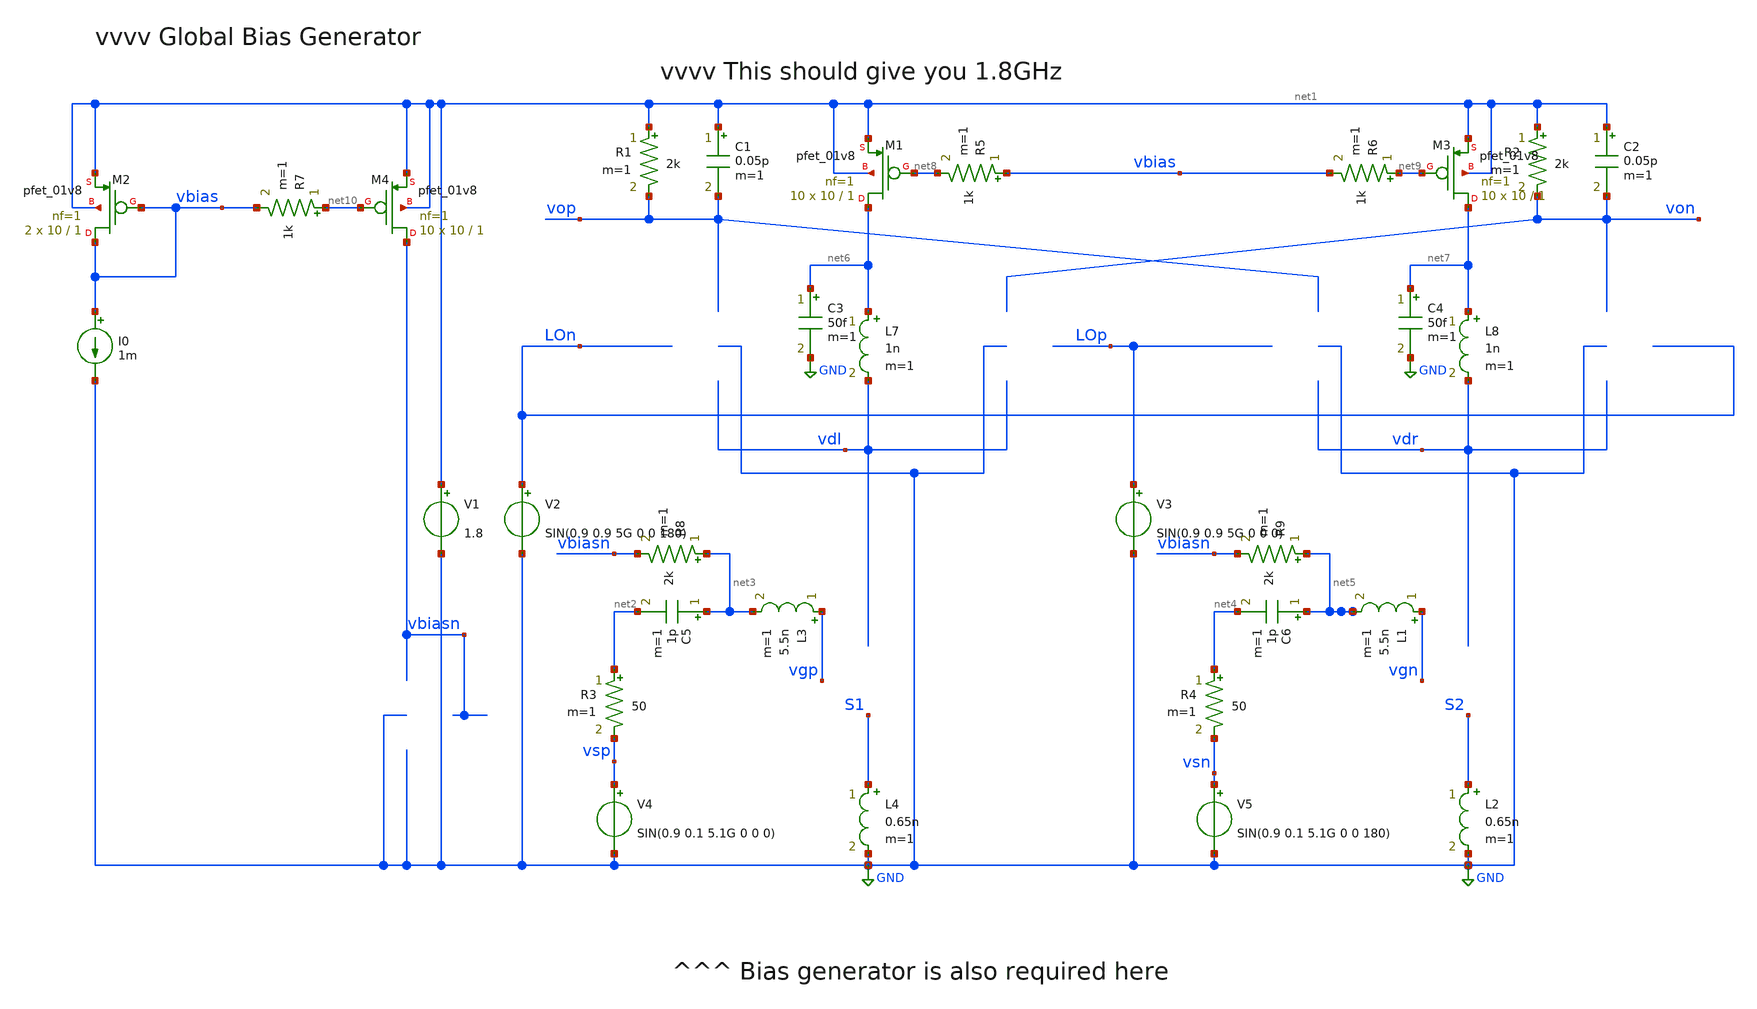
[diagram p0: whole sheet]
** sch_path: xschem/MIXER_5G.sch
**.subckt MIXER_5G
C1 net1 vop 0.05p m=1
R1 net1 vop 2k m=1
C2 net1 von 0.05p m=1
R2 net1 von 2k m=1
V1 net1 GND 1.8
V2 LOn GND SIN(0.9 0.9 5G 0 0 180)
V3 LOp GND SIN(0.9 0.9 5G 0 0 0)
V4 vsp GND SIN(0.9 0.1 5.1G 0 0 0)
V5 vsn GND SIN(0.9 0.1 5.1G 0 0 180)
L3 vgp net3 5.5n m=1
L1 vgn net5 5.5n m=1
L2 S2 GND 0.65n m=1
L4 S1 GND 0.65n m=1
R3 net2 vsp 50 m=1
R4 net4 vsn 50 m=1
L7 net6 vdl 1n m=1
C3 net6 GND 50f m=1
L8 net7 vdr 1n m=1
C4 net7 GND 50f m=1
XM2 vbias vbias net1 net1 sky130_fd_pr__pfet_01v8 L=1 W=10 nf=1 ad='int((nf+1)/2) * W/nf * 0.29' as='int((nf+2)/2) * W/nf * 0.29'
+ pd='2*int((nf+1)/2) * (W/nf + 0.29)' ps='2*int((nf+2)/2) * (W/nf + 0.29)' nrd='0.29 / W' nrs='0.29 / W'
+ sa=0 sb=0 sd=0 mult=2 m=2
I0 vbias GND 1m
XM1 net6 net8 net1 net1 sky130_fd_pr__pfet_01v8 L=1 W=10 nf=1 ad='int((nf+1)/2) * W/nf * 0.29' as='int((nf+2)/2) * W/nf * 0.29'
+ pd='2*int((nf+1)/2) * (W/nf + 0.29)' ps='2*int((nf+2)/2) * (W/nf + 0.29)' nrd='0.29 / W' nrs='0.29 / W'
+ sa=0 sb=0 sd=0 mult=10 m=10
R5 vbias net8 1k m=1
XM3 net7 net9 net1 net1 sky130_fd_pr__pfet_01v8 L=1 W=10 nf=1 ad='int((nf+1)/2) * W/nf * 0.29' as='int((nf+2)/2) * W/nf * 0.29'
+ pd='2*int((nf+1)/2) * (W/nf + 0.29)' ps='2*int((nf+2)/2) * (W/nf + 0.29)' nrd='0.29 / W' nrs='0.29 / W'
+ sa=0 sb=0 sd=0 mult=10 m=10
R6 net9 vbias 1k m=1
XM4 vbiasn net10 net1 net1 sky130_fd_pr__pfet_01v8 L=1 W=10 nf=1 ad='int((nf+1)/2) * W/nf * 0.29' as='int((nf+2)/2) * W/nf * 0.29'
+ pd='2*int((nf+1)/2) * (W/nf + 0.29)' ps='2*int((nf+2)/2) * (W/nf + 0.29)' nrd='0.29 / W' nrs='0.29 / W'
+ sa=0 sb=0 sd=0 mult=10 m=10
R7 net10 vbias 1k m=1
C5 net3 net2 1p m=1
R8 net3 vbiasn 2k m=1
C6 net5 net4 1p m=1
R9 net5 vbiasn 2k m=1
**** begin user architecture code


.subckt sky130_fd_pr__rf_nfet_01v8_bM04W5p00L0p15_ext DRAIN GATE SOURCE SUBSTRATE
X0 DRAIN GATE SOURCE SUBSTRATE sky130_fd_pr__nfet_01v8 ad=2.828e+12p pd=2.132e+07u as=4.242e+12p
+ ps=3.198e+07u w=5.05e+06u l=150000u
X1 SOURCE SUBSTRATE SUBSTRATE SUBSTRATE sky130_fd_pr__nfet_01v8 ad=0p pd=0u as=3.03e+12p
+ ps=2.14e+07u w=5.05e+06u l=150000u
X2 SOURCE GATE DRAIN SUBSTRATE sky130_fd_pr__nfet_01v8 ad=0p pd=0u as=0p ps=0u w=5.05e+06u l=150000u
X3 DRAIN GATE SOURCE SUBSTRATE sky130_fd_pr__nfet_01v8 ad=0p pd=0u as=0p ps=0u w=5.05e+06u l=150000u
X4 SUBSTRATE SUBSTRATE SOURCE SUBSTRATE sky130_fd_pr__nfet_01v8 ad=0p pd=0u as=0p ps=0u w=5.05e+06u
+ l=150000u
X5 SOURCE GATE DRAIN SUBSTRATE sky130_fd_pr__nfet_01v8 ad=0p pd=0u as=0p ps=0u w=5.05e+06u l=150000u
.ends

.subckt NFET_extract D G S B
X0 D G S B sky130_fd_pr__nfet_01v8 ad=0p pd=0u as=0p ps=0u w=5.05e+06u l=150000u
X1 D G S B sky130_fd_pr__nfet_01v8 ad=0p pd=0u as=0p ps=0u w=5.05e+06u l=150000u
X2 S G D B sky130_fd_pr__nfet_01v8 ad=0p pd=0u as=0p ps=0u w=5.05e+06u l=150000u
X3 S G D B sky130_fd_pr__nfet_01v8 ad=0p pd=0u as=0p ps=0u w=5.05e+06u l=150000u
C0 S D 9.91fF
C1 D B 2.61fF
.ends

* Extraction of 6xaM02 (12 finger) Transistors
* wt=60um, L=0.15um
.subckt NFET_extract_1 D G S B

 .subckt sky130_fd_pr__rf_nfet_01v8_aM02W5p00L0p15 DRAIN GATE SOURCE SUBSTRATE
  X0 DRAIN GATE SOURCE SUBSTRATE sky130_fd_pr__nfet_01v8 ad=1.414e+12p pd=1.066e+07u as=2.828e+12p
+ ps=2.132e+07u w=5.05e+06u l=150000u
  X1 SOURCE GATE DRAIN SUBSTRATE sky130_fd_pr__nfet_01v8 ad=0p pd=0u as=0p ps=0u w=5.05e+06u
+ l=150000u
  C0 SOURCE DRAIN 3.73fF
  C1 SOURCE SUBSTRATE 2.58fF
 .ends

C0 B G 2.85fF
C1 S D 22.23fF
C2 G D 5.77fF
C3 S G 7.53fF
Xnfet_3x_2_0/sky130_fd_pr__rf_nfet_01v8_aM02W5p00L0p15_0 D G S B
+ sky130_fd_pr__rf_nfet_01v8_aM02W5p00L0p15
Xnfet_3x_2_0/sky130_fd_pr__rf_nfet_01v8_aM02W5p00L0p15_1 D G S B
+ sky130_fd_pr__rf_nfet_01v8_aM02W5p00L0p15
Xnfet_3x_2_0/sky130_fd_pr__rf_nfet_01v8_aM02W5p00L0p15_2 D G S B
+ sky130_fd_pr__rf_nfet_01v8_aM02W5p00L0p15
Xnfet_3x_2_1/sky130_fd_pr__rf_nfet_01v8_aM02W5p00L0p15_0 D G S B
+ sky130_fd_pr__rf_nfet_01v8_aM02W5p00L0p15
Xnfet_3x_2_1/sky130_fd_pr__rf_nfet_01v8_aM02W5p00L0p15_1 D G S B
+ sky130_fd_pr__rf_nfet_01v8_aM02W5p00L0p15
Xnfet_3x_2_1/sky130_fd_pr__rf_nfet_01v8_aM02W5p00L0p15_2 D G S B
+ sky130_fd_pr__rf_nfet_01v8_aM02W5p00L0p15
C4 S B 13.70fF
C5 G B 3.35fF

.ends


XMEXT_0_0 vdl vgp S1 GND NFET_extract_1
XMEXT_0_1 vdl vgp S1 GND NFET_extract_1

XMEXT_1_0 vdr vgn S2 GND NFET_extract_1
XMEXT_1_1 vdr vgn S2 GND NFET_extract_1

XMEXT_l1_0 vop LOn vdl GND NFET_extract_1
XMEXT_l2_0 von LOp vdl GND NFET_extract_1
XMEXT_r1_0 vop LOp vdr GND NFET_extract_1
XMEXT_r2_0 von LOn vdr GND NFET_extract_1

XMEXT_l1_1 vop LOn vdl GND NFET_extract_1
XMEXT_l2_1 von LOp vdl GND NFET_extract_1
XMEXT_r1_1 vop LOp vdr GND NFET_extract_1
XMEXT_r2_1 von LOn vdr GND NFET_extract_1
.options savecurrents

.tran 10ps 50ns
.control
run
display
*let m_start = 9
*let m_stop  = 14
*let m_delta = 1
let vo = v(vop)-v(von)
let vs = v(vsp)-v(vsn)
let vg = v(vgp)-v(vgn)

*let m_var = m_start
*while m_var le m_stop
*  print m_var
*  alter @m.xm1.msky130_fd_pr__pfet_01v8[m] = m_var
*  alter @m.xm3.msky130_fd_pr__pfet_01v8[m] = m_var

*  tran 10ps 50ns
*  * plot v(von) v(vop)
*  let vo = v(vop)-v(von)
plot @l7[i]
plot vo
*  let m_var = m_var + m_delta
*end


* plot vo
plot vs
plot vg
* fft vo vs vg
* plot db(vo) db(vs)



.endc


.lib $::SKYWATER_MODELS/sky130.lib.spice tt
* .include $::PDKPATH/libs.ref/sky130_fd_sc_hvl/spice/sky130_fd_sc_hvl.spice

**** end user architecture code
**.ends
.GLOBAL GND
.end
